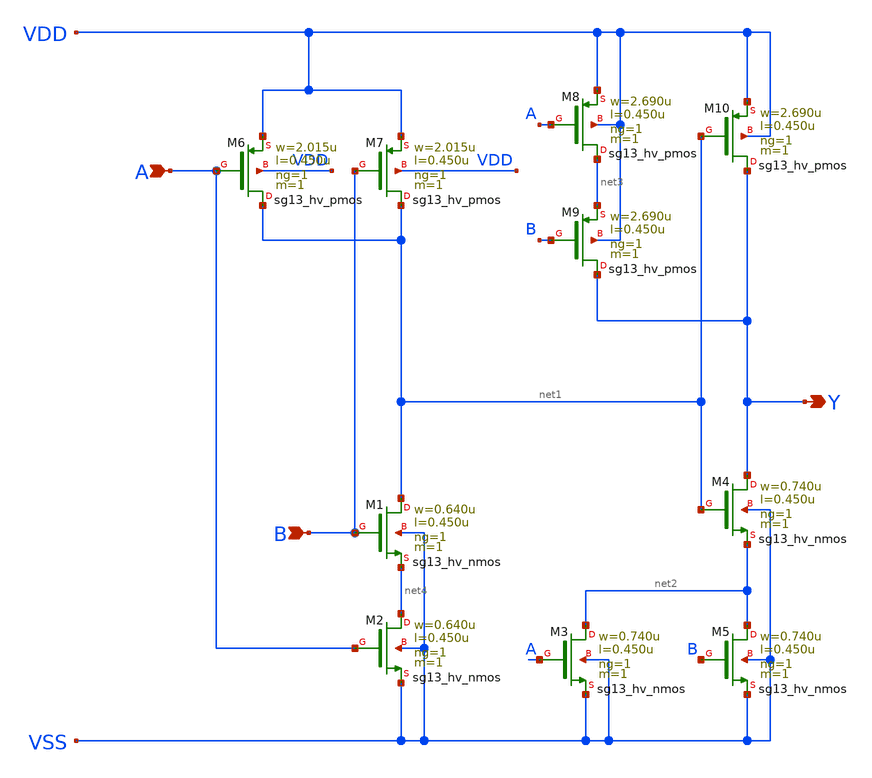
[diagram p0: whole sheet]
** sch_path: ihp-sg13g2/libs.ref/sg13g2_stdcell_hv/sch/xschem/sg13g2_hv_xnor2_1.sch
* Copyright 2023 IHP PDK Authors
* Licensed under the Apache License, Version 2.0 (the "License");
* you may not use this file except in compliance with the License.
* You may obtain a copy of the License at
* https://www.apache.org/licenses/LICENSE-2.0
* Unless required by applicable law or agreed to in writing, software
* distributed under the License is distributed on an "AS IS" BASIS,
* WITHOUT WARRANTIES OR CONDITIONS OF ANY KIND, either express or implied.
* See the License for the specific language governing permissions and
* limitations under the License.
**.subckt sg13g2_hv_xnor2_1 A Y B
*.ipin A
*.opin Y
*.ipin B
XM1 net1 B net4 VSS sg13_hv_nmos w=0.640u l=0.450u ng=1 m=1 mm_ok=1
XM2 net4 A VSS VSS sg13_hv_nmos w=0.640u l=0.450u ng=1 m=1 mm_ok=1
XM3 net2 A VSS VSS sg13_hv_nmos w=0.740u l=0.450u ng=1 m=1 mm_ok=1
XM4 Y net1 net2 VSS sg13_hv_nmos w=0.740u l=0.450u ng=1 m=1 mm_ok=1
XM5 net2 B VSS VSS sg13_hv_nmos w=0.740u l=0.450u ng=1 m=1 mm_ok=1
XM6 net1 A VDD VDD sg13_hv_pmos w=2.015u l=0.450u ng=1 m=1 mm_ok=1
XM7 net1 B VDD VDD sg13_hv_pmos w=2.015u l=0.450u ng=1 m=1 mm_ok=1
XM8 net3 A VDD VDD sg13_hv_pmos w=2.690u l=0.450u ng=1 m=1 mm_ok=1
XM9 Y B net3 VDD sg13_hv_pmos w=2.690u l=0.450u ng=1 m=1 mm_ok=1
XM10 Y net1 VDD VDD sg13_hv_pmos w=2.690u l=0.450u ng=1 m=1 mm_ok=1
**.ends
.end
